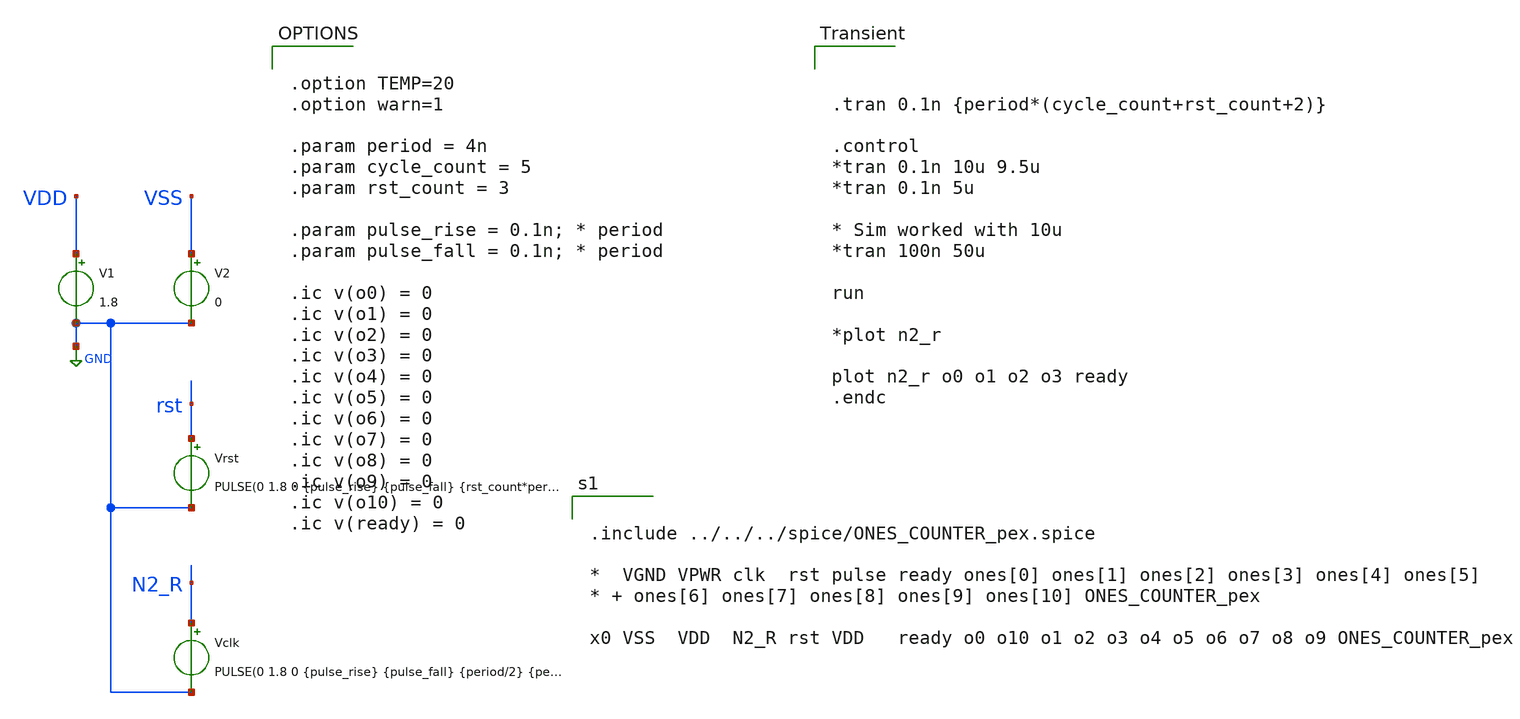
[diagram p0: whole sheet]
** sch_path: modules/ONES_COUNTER/test/pex_counter.sch
**.subckt pex_counter
V1 VDD GND 1.8
V2 VSS GND 0
Vrst rst GND PULSE(0 1.8 0 {pulse_rise} {pulse_fall} {rst_count*period} {rst_count*period} 1)
Vclk N2_R GND PULSE(0 1.8 0 {pulse_rise} {pulse_fall} {period/2} {period})
**** begin user architecture code



.tran 0.1n {period*(cycle_count+rst_count+2)}

.control
*tran 0.1n 10u 9.5u
*tran 0.1n 5u

* Sim worked with 10u
*tran 100n 50u

run

*plot n2_r

plot n2_r o0 o1 o2 o3 ready
.endc



.option TEMP=20
.option warn=1

.param period = 4n
.param cycle_count = 5
.param rst_count = 3

.param pulse_rise = 0.1n; * period
.param pulse_fall = 0.1n; * period

.ic v(o0) = 0
.ic v(o1) = 0
.ic v(o2) = 0
.ic v(o3) = 0
.ic v(o4) = 0
.ic v(o5) = 0
.ic v(o6) = 0
.ic v(o7) = 0
.ic v(o8) = 0
.ic v(o9) = 0
.ic v(o10) = 0
.ic v(ready) = 0



*.lib $env(PDK_ROOT)/$env(PDK)/libs.tech/combined/sky130.lib.spice tt
.lib $env(PDK_ROOT)/$env(PDK)/libs.tech/ngspice/sky130.lib.spice tt

*.include $env(PDK_ROOT)/$env(PDK)/libs.ref/sky130_fd_sc_hd/spice/sky130_fd_sc_hd.spice



.include ../../../spice/ONES_COUNTER_pex.spice

*  VGND VPWR clk  rst pulse ready ones[0] ones[1] ones[2] ones[3] ones[4] ones[5]
* + ones[6] ones[7] ones[8] ones[9] ones[10] ONES_COUNTER_pex

x0 VSS  VDD  N2_R rst VDD   ready o0 o10 o1 o2 o3 o4 o5 o6 o7 o8 o9 ONES_COUNTER_pex


**** end user architecture code
**.ends
.GLOBAL GND
.end
